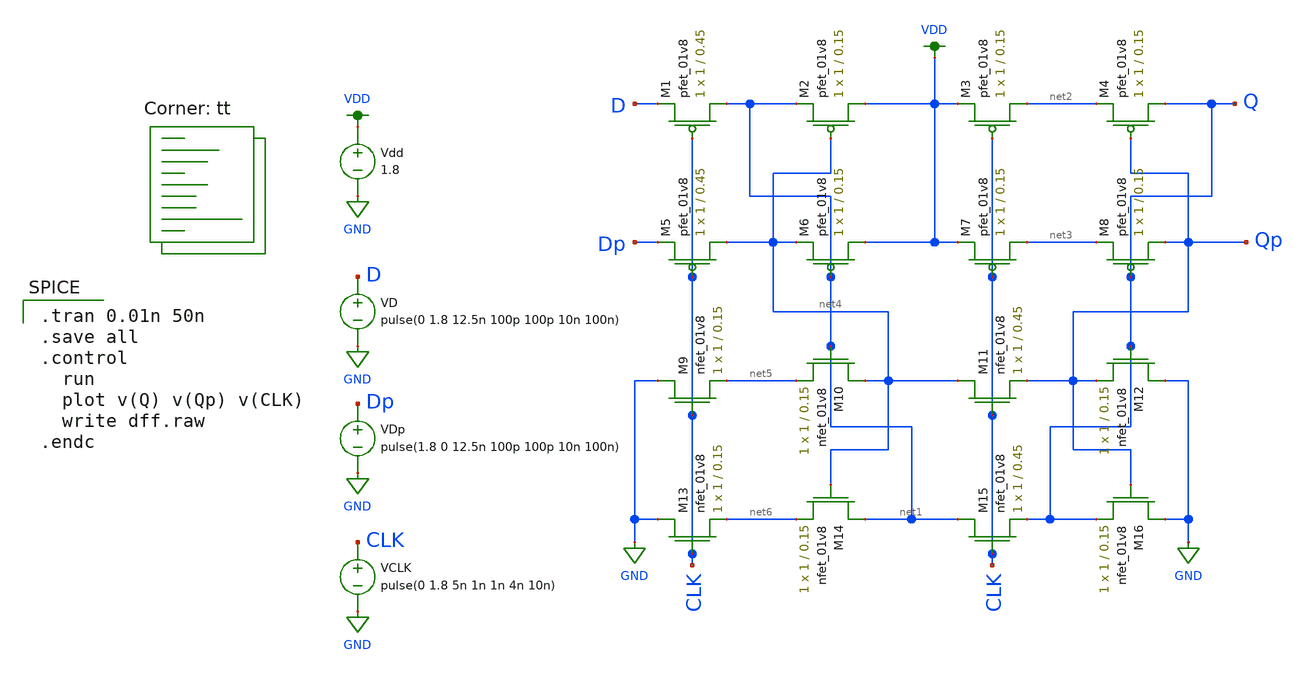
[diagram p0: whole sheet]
** sch_path: mp2/dff_tb.sch
**.subckt dff_tb
Vdd VDD GND 1.8
XM1 net1 CLK D VDD sky130_fd_pr__pfet_01v8 L=0.45 W=1 nf=1 ad='int((nf+1)/2) * W/nf * 0.29' as='int((nf+2)/2) * W/nf * 0.29'
+ pd='2*int((nf+1)/2) * (W/nf + 0.29)' ps='2*int((nf+2)/2) * (W/nf + 0.29)' nrd='0.29 / W' nrs='0.29 / W'
+ sa=0 sb=0 sd=0 mult=1 m=1
XM2 VDD net4 net1 VDD sky130_fd_pr__pfet_01v8 L=0.15 W=1 nf=1 ad='int((nf+1)/2) * W/nf * 0.29' as='int((nf+2)/2) * W/nf * 0.29'
+ pd='2*int((nf+1)/2) * (W/nf + 0.29)' ps='2*int((nf+2)/2) * (W/nf + 0.29)' nrd='0.29 / W' nrs='0.29 / W'
+ sa=0 sb=0 sd=0 mult=1 m=1
XM3 net2 CLK VDD VDD sky130_fd_pr__pfet_01v8 L=0.15 W=1 nf=1 ad='int((nf+1)/2) * W/nf * 0.29' as='int((nf+2)/2) * W/nf * 0.29'
+ pd='2*int((nf+1)/2) * (W/nf + 0.29)' ps='2*int((nf+2)/2) * (W/nf + 0.29)' nrd='0.29 / W' nrs='0.29 / W'
+ sa=0 sb=0 sd=0 mult=1 m=1
XM4 Q Qp net2 VDD sky130_fd_pr__pfet_01v8 L=0.15 W=1 nf=1 ad='int((nf+1)/2) * W/nf * 0.29' as='int((nf+2)/2) * W/nf * 0.29'
+ pd='2*int((nf+1)/2) * (W/nf + 0.29)' ps='2*int((nf+2)/2) * (W/nf + 0.29)' nrd='0.29 / W' nrs='0.29 / W'
+ sa=0 sb=0 sd=0 mult=1 m=1
XM5 net4 CLK Dp VDD sky130_fd_pr__pfet_01v8 L=0.45 W=1 nf=1 ad='int((nf+1)/2) * W/nf * 0.29' as='int((nf+2)/2) * W/nf * 0.29'
+ pd='2*int((nf+1)/2) * (W/nf + 0.29)' ps='2*int((nf+2)/2) * (W/nf + 0.29)' nrd='0.29 / W' nrs='0.29 / W'
+ sa=0 sb=0 sd=0 mult=1 m=1
XM6 VDD net1 net4 VDD sky130_fd_pr__pfet_01v8 L=0.15 W=1 nf=1 ad='int((nf+1)/2) * W/nf * 0.29' as='int((nf+2)/2) * W/nf * 0.29'
+ pd='2*int((nf+1)/2) * (W/nf + 0.29)' ps='2*int((nf+2)/2) * (W/nf + 0.29)' nrd='0.29 / W' nrs='0.29 / W'
+ sa=0 sb=0 sd=0 mult=1 m=1
XM7 net3 CLK VDD VDD sky130_fd_pr__pfet_01v8 L=0.15 W=1 nf=1 ad='int((nf+1)/2) * W/nf * 0.29' as='int((nf+2)/2) * W/nf * 0.29'
+ pd='2*int((nf+1)/2) * (W/nf + 0.29)' ps='2*int((nf+2)/2) * (W/nf + 0.29)' nrd='0.29 / W' nrs='0.29 / W'
+ sa=0 sb=0 sd=0 mult=1 m=1
XM8 Qp Q net3 VDD sky130_fd_pr__pfet_01v8 L=0.15 W=1 nf=1 ad='int((nf+1)/2) * W/nf * 0.29' as='int((nf+2)/2) * W/nf * 0.29'
+ pd='2*int((nf+1)/2) * (W/nf + 0.29)' ps='2*int((nf+2)/2) * (W/nf + 0.29)' nrd='0.29 / W' nrs='0.29 / W'
+ sa=0 sb=0 sd=0 mult=1 m=1
XM9 GND CLK net5 GND sky130_fd_pr__nfet_01v8 L=0.15 W=1 nf=1 ad='int((nf+1)/2) * W/nf * 0.29' as='int((nf+2)/2) * W/nf * 0.29'
+ pd='2*int((nf+1)/2) * (W/nf + 0.29)' ps='2*int((nf+2)/2) * (W/nf + 0.29)' nrd='0.29 / W' nrs='0.29 / W'
+ sa=0 sb=0 sd=0 mult=1 m=1
XM10 net4 net1 net5 GND sky130_fd_pr__nfet_01v8 L=0.15 W=1 nf=1 ad='int((nf+1)/2) * W/nf * 0.29' as='int((nf+2)/2) * W/nf * 0.29'
+ pd='2*int((nf+1)/2) * (W/nf + 0.29)' ps='2*int((nf+2)/2) * (W/nf + 0.29)' nrd='0.29 / W' nrs='0.29 / W'
+ sa=0 sb=0 sd=0 mult=1 m=1
XM11 net4 CLK Qp GND sky130_fd_pr__nfet_01v8 L=0.45 W=1 nf=1 ad='int((nf+1)/2) * W/nf * 0.29' as='int((nf+2)/2) * W/nf * 0.29'
+ pd='2*int((nf+1)/2) * (W/nf + 0.29)' ps='2*int((nf+2)/2) * (W/nf + 0.29)' nrd='0.29 / W' nrs='0.29 / W'
+ sa=0 sb=0 sd=0 mult=1 m=1
XM12 GND Q Qp GND sky130_fd_pr__nfet_01v8 L=0.15 W=1 nf=1 ad='int((nf+1)/2) * W/nf * 0.29' as='int((nf+2)/2) * W/nf * 0.29'
+ pd='2*int((nf+1)/2) * (W/nf + 0.29)' ps='2*int((nf+2)/2) * (W/nf + 0.29)' nrd='0.29 / W' nrs='0.29 / W'
+ sa=0 sb=0 sd=0 mult=1 m=1
XM13 GND CLK net6 GND sky130_fd_pr__nfet_01v8 L=0.15 W=1 nf=1 ad='int((nf+1)/2) * W/nf * 0.29' as='int((nf+2)/2) * W/nf * 0.29'
+ pd='2*int((nf+1)/2) * (W/nf + 0.29)' ps='2*int((nf+2)/2) * (W/nf + 0.29)' nrd='0.29 / W' nrs='0.29 / W'
+ sa=0 sb=0 sd=0 mult=1 m=1
XM14 net1 net4 net6 GND sky130_fd_pr__nfet_01v8 L=0.15 W=1 nf=1 ad='int((nf+1)/2) * W/nf * 0.29' as='int((nf+2)/2) * W/nf * 0.29'
+ pd='2*int((nf+1)/2) * (W/nf + 0.29)' ps='2*int((nf+2)/2) * (W/nf + 0.29)' nrd='0.29 / W' nrs='0.29 / W'
+ sa=0 sb=0 sd=0 mult=1 m=1
XM15 net1 CLK Q GND sky130_fd_pr__nfet_01v8 L=0.45 W=1 nf=1 ad='int((nf+1)/2) * W/nf * 0.29' as='int((nf+2)/2) * W/nf * 0.29'
+ pd='2*int((nf+1)/2) * (W/nf + 0.29)' ps='2*int((nf+2)/2) * (W/nf + 0.29)' nrd='0.29 / W' nrs='0.29 / W'
+ sa=0 sb=0 sd=0 mult=1 m=1
XM16 GND Qp Q GND sky130_fd_pr__nfet_01v8 L=0.15 W=1 nf=1 ad='int((nf+1)/2) * W/nf * 0.29' as='int((nf+2)/2) * W/nf * 0.29'
+ pd='2*int((nf+1)/2) * (W/nf + 0.29)' ps='2*int((nf+2)/2) * (W/nf + 0.29)' nrd='0.29 / W' nrs='0.29 / W'
+ sa=0 sb=0 sd=0 mult=1 m=1
VD D GND pulse(0 1.8 12.5n 100p 100p 10n 100n)
VDp Dp GND pulse(1.8 0 12.5n 100p 100p 10n 100n)
VCLK CLK GND pulse(0 1.8 5n 1n 1n 4n 10n)
**** begin user architecture code
.lib $::SKYWATER_MODELS/sky130.lib.spice tt

.tran 0.01n 50n
.save all
.control
  run
  plot v(Q) v(Qp) v(CLK)
  write dff.raw
.endc

**** end user architecture code
**.ends
.GLOBAL VDD
.GLOBAL GND
.end
